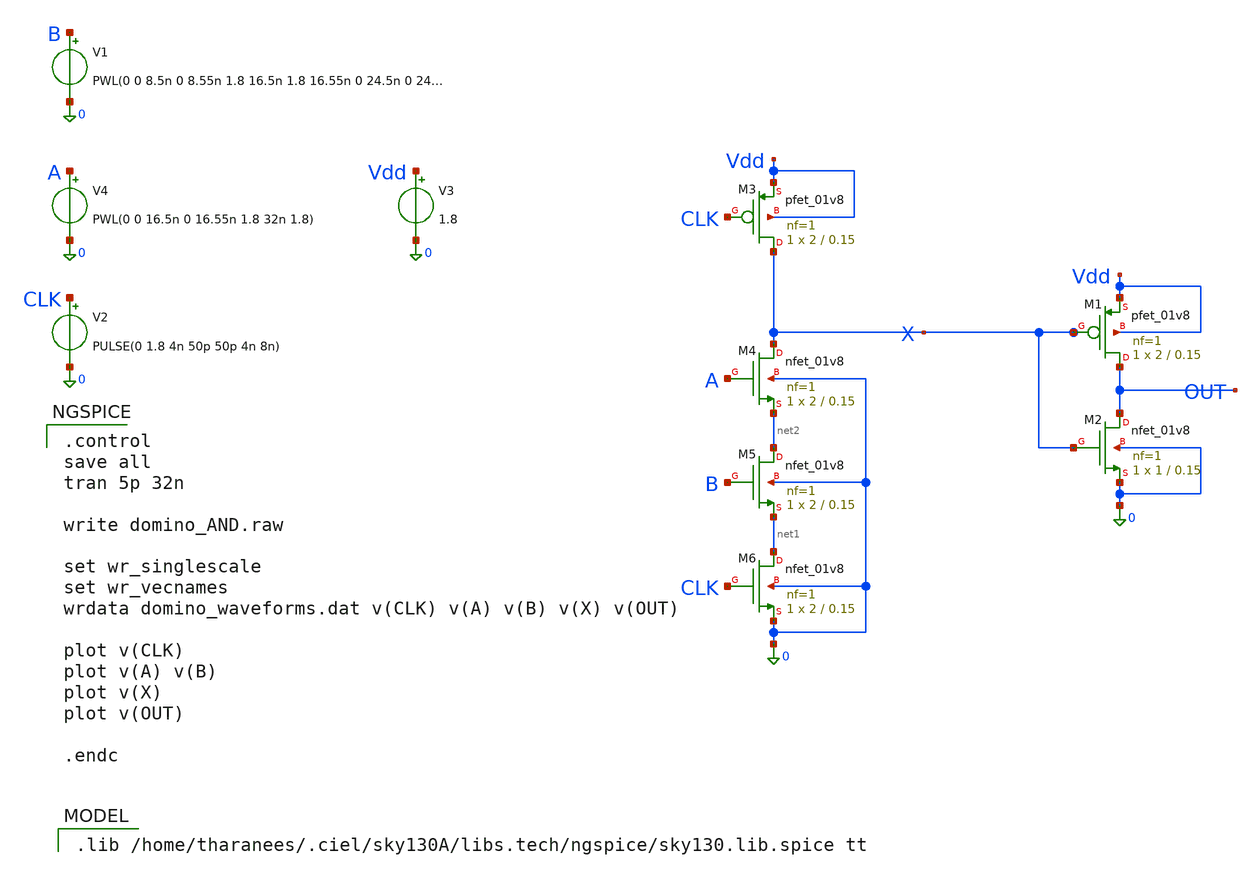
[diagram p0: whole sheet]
** sch_path: domino_AND.sch
**.subckt domino_AND
XM1 OUT X Vdd Vdd sky130_fd_pr__pfet_01v8 L=0.15 W=2 nf=1 ad=0.58 as=0.58 pd=4.58 ps=4.58 nrd=0.145
+ nrs=0.145 sa=0 sb=0 sd=0 mult=1 m=1
XM2 OUT X 0 0 sky130_fd_pr__nfet_01v8 L=0.15 W=1 nf=1 ad=0.29 as=0.29 pd=2.58 ps=2.58 nrd=0.29
+ nrs=0.29 sa=0 sb=0 sd=0 mult=1 m=1
V2 CLK 0 PULSE(0 1.8 4n 50p 50p 4n 8n)
V3 Vdd 0 1.8
XM3 X CLK Vdd Vdd sky130_fd_pr__pfet_01v8 L=0.15 W=2 nf=1 ad=0.58 as=0.58 pd=4.58 ps=4.58 nrd=0.145
+ nrs=0.145 sa=0 sb=0 sd=0 mult=1 m=1
XM4 X A net2 0 sky130_fd_pr__nfet_01v8 L=0.15 W=2 nf=1 ad=0.58 as=0.58 pd=4.58 ps=4.58 nrd=0.145
+ nrs=0.145 sa=0 sb=0 sd=0 mult=1 m=1
XM5 net2 B net1 0 sky130_fd_pr__nfet_01v8 L=0.15 W=2 nf=1 ad=0.58 as=0.58 pd=4.58 ps=4.58 nrd=0.145
+ nrs=0.145 sa=0 sb=0 sd=0 mult=1 m=1
XM6 net1 CLK 0 0 sky130_fd_pr__nfet_01v8 L=0.15 W=2 nf=1 ad=0.58 as=0.58 pd=4.58 ps=4.58 nrd=0.145
+ nrs=0.145 sa=0 sb=0 sd=0 mult=1 m=1
V1 B 0 PWL(0 0 8.5n 0 8.55n 1.8 16.5n 1.8 16.55n 0 24.5n 0 24.55n 1.8 32n 1.8)
V4 A 0 PWL(0 0 16.5n 0 16.55n 1.8 32n 1.8)
**** begin user architecture code

.lib /home/tharanees/.ciel/sky130A/libs.tech/ngspice/sky130.lib.spice tt


.control
save all
tran 5p 32n

write domino_AND.raw

set wr_singlescale
set wr_vecnames
wrdata domino_waveforms.dat v(CLK) v(A) v(B) v(X) v(OUT)

plot v(CLK)
plot v(A) v(B)
plot v(X)
plot v(OUT)

.endc

**** end user architecture code
**.ends
.end
